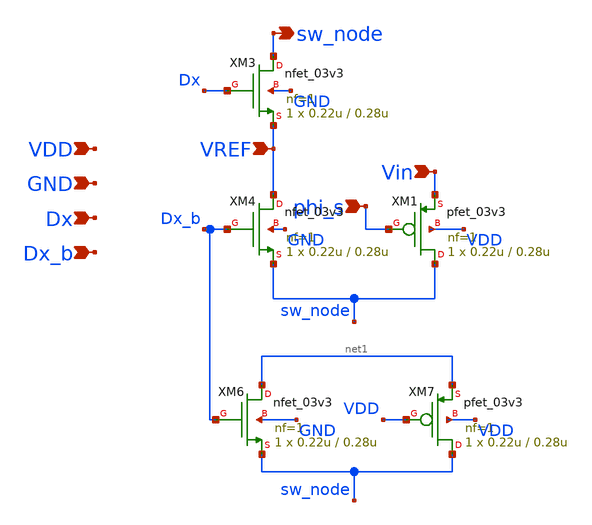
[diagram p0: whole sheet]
** sch_path: analog/blocks/cdac/og_transistors.sch
**.subckt og_transistors sw_node VDD GND Dx Dx_b phi_s VREF Vin
*.opin sw_node
*.ipin VDD
*.ipin GND
*.ipin Dx
*.ipin Dx_b
*.ipin phi_s
*.ipin VREF
*.ipin Vin
XM6 net1 Dx_b sw_node GND nfet_03v3 L=0.28u W=0.22u nf=1 ad='int((nf+1)/2) * W/nf * 0.18u' as='int((nf+2)/2) * W/nf * 0.18u'
+ pd='2*int((nf+1)/2) * (W/nf + 0.18u)' ps='2*int((nf+2)/2) * (W/nf + 0.18u)' nrd='0.18u / W' nrs='0.18u / W'
+ sa=0 sb=0 sd=0 m=1
XM7 sw_node VDD net1 VDD pfet_03v3 L=0.28u W=0.22u nf=1 ad='int((nf+1)/2) * W/nf * 0.18u' as='int((nf+2)/2) * W/nf * 0.18u'
+ pd='2*int((nf+1)/2) * (W/nf + 0.18u)' ps='2*int((nf+2)/2) * (W/nf + 0.18u)' nrd='0.18u / W' nrs='0.18u / W'
+ sa=0 sb=0 sd=0 m=1
XM1 sw_node phi_s Vin VDD pfet_03v3 L=0.28u W=0.22u nf=1 ad='int((nf+1)/2) * W/nf * 0.18u' as='int((nf+2)/2) * W/nf * 0.18u'
+ pd='2*int((nf+1)/2) * (W/nf + 0.18u)' ps='2*int((nf+2)/2) * (W/nf + 0.18u)' nrd='0.18u / W' nrs='0.18u / W'
+ sa=0 sb=0 sd=0 m=1
XM4 VREF Dx_b sw_node GND nfet_03v3 L=0.28u W=0.22u nf=1 ad='int((nf+1)/2) * W/nf * 0.18u' as='int((nf+2)/2) * W/nf * 0.18u'
+ pd='2*int((nf+1)/2) * (W/nf + 0.18u)' ps='2*int((nf+2)/2) * (W/nf + 0.18u)' nrd='0.18u / W' nrs='0.18u / W'
+ sa=0 sb=0 sd=0 m=1
XM3 sw_node Dx VREF GND nfet_03v3 L=0.28u W=0.22u nf=1 ad='int((nf+1)/2) * W/nf * 0.18u' as='int((nf+2)/2) * W/nf * 0.18u'
+ pd='2*int((nf+1)/2) * (W/nf + 0.18u)' ps='2*int((nf+2)/2) * (W/nf + 0.18u)' nrd='0.18u / W' nrs='0.18u / W'
+ sa=0 sb=0 sd=0 m=1
**.ends
.end
